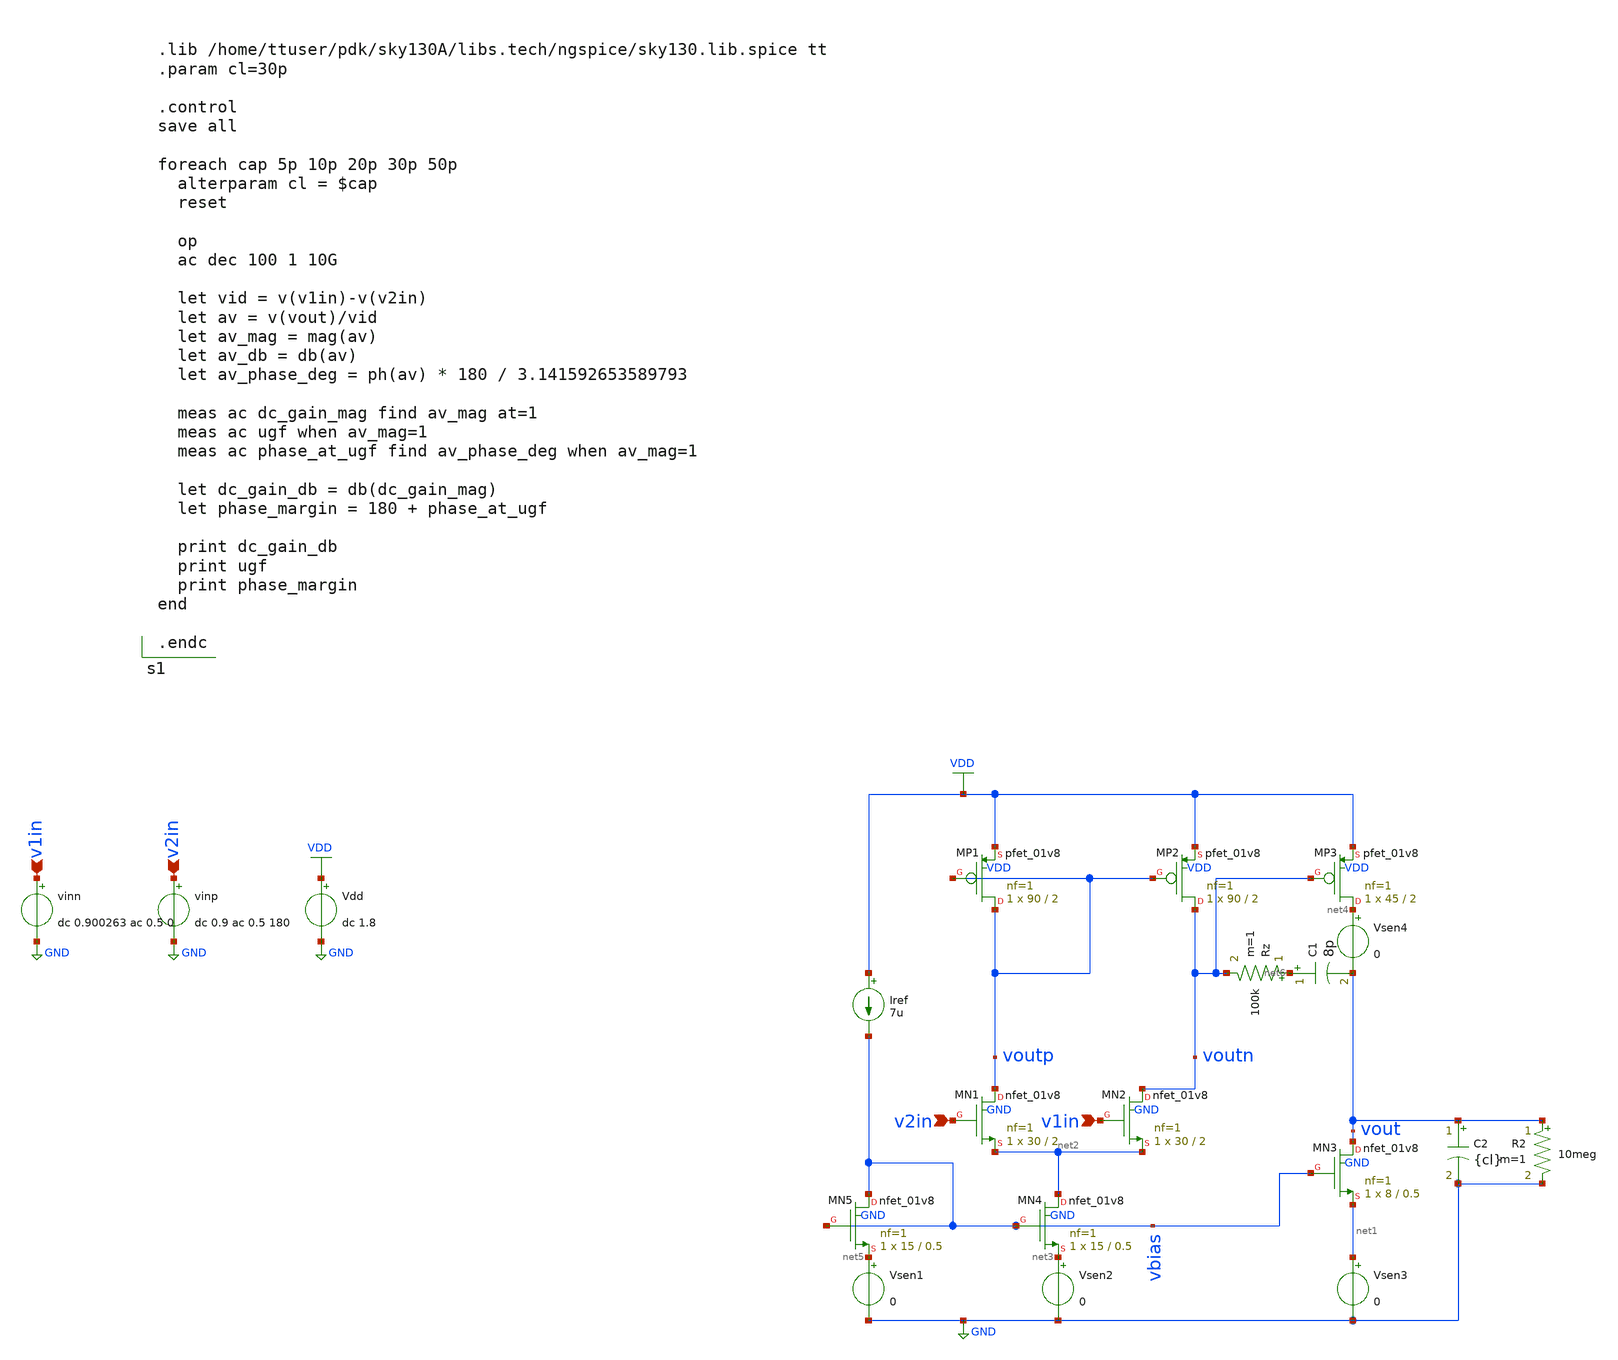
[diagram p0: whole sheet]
** sch_path: testbenches/prelayout/diffpairCLSweep.sch
**.subckt diffpairCLSweep v1in v1in v2in v2in
*.ipin v1in
*.ipin v1in
*.ipin v2in
*.ipin v2in
Vdd VDD GND dc 1.8
vinp v2in GND dc 0.9 ac 0.5 180
vinn v1in GND dc 0.900263 ac 0.5 0
XMN1 voutp v2in net2 GND sky130_fd_pr__nfet_01v8 L=2 W=30 nf=1 ad='int((nf+1)/2) * W/nf * 0.29' as='int((nf+2)/2) * W/nf * 0.29'
+ pd='2*int((nf+1)/2) * (W/nf + 0.29)' ps='2*int((nf+2)/2) * (W/nf + 0.29)' nrd='0.29 / W' nrs='0.29 / W'
+ sa=0 sb=0 sd=0 mult=1 m=1
XMN2 voutn v1in net2 GND sky130_fd_pr__nfet_01v8 L=2 W=30 nf=1 ad='int((nf+1)/2) * W/nf * 0.29' as='int((nf+2)/2) * W/nf * 0.29'
+ pd='2*int((nf+1)/2) * (W/nf + 0.29)' ps='2*int((nf+2)/2) * (W/nf + 0.29)' nrd='0.29 / W' nrs='0.29 / W'
+ sa=0 sb=0 sd=0 mult=1 m=1
XMP1 voutp voutp VDD VDD sky130_fd_pr__pfet_01v8 L=2 W=90 nf=1 ad='int((nf+1)/2) * W/nf * 0.29' as='int((nf+2)/2) * W/nf * 0.29'
+ pd='2*int((nf+1)/2) * (W/nf + 0.29)' ps='2*int((nf+2)/2) * (W/nf + 0.29)' nrd='0.29 / W' nrs='0.29 / W'
+ sa=0 sb=0 sd=0 mult=1 m=1
XMP2 voutn voutp VDD VDD sky130_fd_pr__pfet_01v8 L=2 W=90 nf=1 ad='int((nf+1)/2) * W/nf * 0.29' as='int((nf+2)/2) * W/nf * 0.29'
+ pd='2*int((nf+1)/2) * (W/nf + 0.29)' ps='2*int((nf+2)/2) * (W/nf + 0.29)' nrd='0.29 / W' nrs='0.29 / W'
+ sa=0 sb=0 sd=0 mult=1 m=1
Iref VDD vbias 7u
Vsen2 net3 GND 0
XMP3 net4 voutn VDD VDD sky130_fd_pr__pfet_01v8 L=2 W=45 nf=1 ad='int((nf+1)/2) * W/nf * 0.29' as='int((nf+2)/2) * W/nf * 0.29'
+ pd='2*int((nf+1)/2) * (W/nf + 0.29)' ps='2*int((nf+2)/2) * (W/nf + 0.29)' nrd='0.29 / W' nrs='0.29 / W'
+ sa=0 sb=0 sd=0 mult=1 m=1
XMN3 vout vbias net1 GND sky130_fd_pr__nfet_01v8 L=0.5 W=8 nf=1 ad='int((nf+1)/2) * W/nf * 0.29' as='int((nf+2)/2) * W/nf * 0.29'
+ pd='2*int((nf+1)/2) * (W/nf + 0.29)' ps='2*int((nf+2)/2) * (W/nf + 0.29)' nrd='0.29 / W' nrs='0.29 / W'
+ sa=0 sb=0 sd=0 mult=1 m=1
Vsen3 net1 GND 0
Vsen1 net5 GND 0
C1 net6 vout 8p m=1
XMN4 net2 vbias net3 GND sky130_fd_pr__nfet_01v8 L=0.5 W=15 nf=1 ad='int((nf+1)/2) * W/nf * 0.29' as='int((nf+2)/2) * W/nf * 0.29'
+ pd='2*int((nf+1)/2) * (W/nf + 0.29)' ps='2*int((nf+2)/2) * (W/nf + 0.29)' nrd='0.29 / W' nrs='0.29 / W'
+ sa=0 sb=0 sd=0 mult=1 m=1
XMN5 vbias vbias net5 GND sky130_fd_pr__nfet_01v8 L=0.5 W=15 nf=1 ad='int((nf+1)/2) * W/nf * 0.29' as='int((nf+2)/2) * W/nf * 0.29'
+ pd='2*int((nf+1)/2) * (W/nf + 0.29)' ps='2*int((nf+2)/2) * (W/nf + 0.29)' nrd='0.29 / W' nrs='0.29 / W'
+ sa=0 sb=0 sd=0 mult=1 m=1
C2 vout GND {cl} m=1
Rz net6 voutn 100k m=1
Vsen4 net4 vout 0
R2 vout GND 10meg m=1
**** begin user architecture code


.lib /home/ttuser/pdk/sky130A/libs.tech/ngspice/sky130.lib.spice tt
.param cl=30p

.control
save all

foreach cap 5p 10p 20p 30p 50p
  alterparam cl = $cap
  reset

  op
  ac dec 100 1 10G

  let vid = v(v1in)-v(v2in)
  let av = v(vout)/vid
  let av_mag = mag(av)
  let av_db = db(av)
  let av_phase_deg = ph(av) * 180 / 3.141592653589793

  meas ac dc_gain_mag find av_mag at=1
  meas ac ugf when av_mag=1
  meas ac phase_at_ugf find av_phase_deg when av_mag=1

  let dc_gain_db = db(dc_gain_mag)
  let phase_margin = 180 + phase_at_ugf

  print dc_gain_db
  print ugf
  print phase_margin
end

.endc


**** end user architecture code
**.ends
.GLOBAL VDD
.GLOBAL GND
.end
